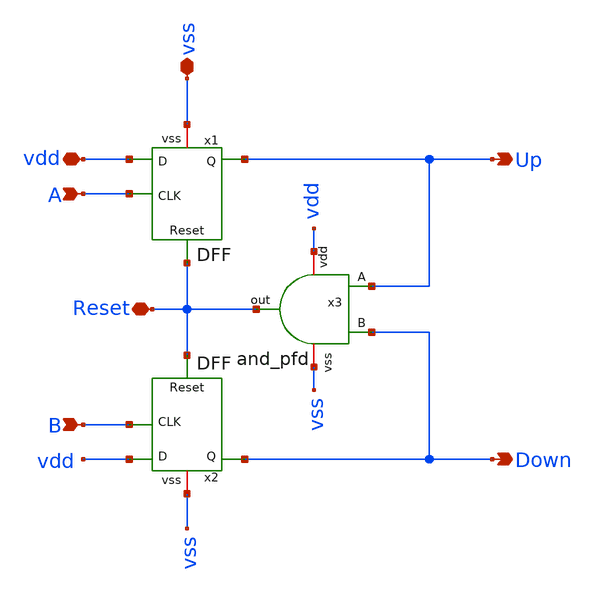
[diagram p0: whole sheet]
** sch_path: xschem/PFD.sch
**.subckt PFD vdd vss A B Down Up Reset
*.iopin vdd
*.iopin vss
*.ipin A
*.ipin B
*.opin Down
*.opin Up
*.iopin Reset
x1 vdd A Up Reset vss DFF
x2 vdd B Down Reset vss DFF
x3 vdd Reset Up Down vss and_pfd
**.ends

* expanding   symbol:  DFF.sym # of pins=5
** sym_path: xschem/DFF.sym
** sch_path: xschem/DFF.sch
.subckt DFF D CLK Q Reset vss
*.ipin D
*.ipin CLK
*.opin Q
*.ipin Reset
*.iopin vss
x1 D CLK Q P vss nor
x2 D P P1 Q vss nor
x3 D P P2 P1 vss nor
x4 D P1 Reset P2 vss nor
.ends


* expanding   symbol:  and_pfd.sym # of pins=5
** sym_path: xschem/and_pfd.sym
** sch_path: xschem/and_pfd.sch
.subckt and_pfd vdd out A B vss
*.iopin vdd
*.iopin vss
*.opin out
*.ipin A
*.ipin B
XM1 out_nand A net1 vss sky130_fd_pr__nfet_01v8 L=0.15 W=0.45 nf=1 ad='int((nf+1)/2) * W/nf * 0.29' as='int((nf+2)/2) * W/nf * 0.29'
+ pd='2*int((nf+1)/2) * (W/nf + 0.29)' ps='2*int((nf+2)/2) * (W/nf + 0.29)' nrd='0.29 / W' nrs='0.29 / W'
+ sa=0 sb=0 sd=0 mult=1 m=1
XM2 out_nand A vdd vdd sky130_fd_pr__pfet_01v8 L=0.15 W=0.9 nf=1 ad='int((nf+1)/2) * W/nf * 0.29' as='int((nf+2)/2) * W/nf * 0.29'
+ pd='2*int((nf+1)/2) * (W/nf + 0.29)' ps='2*int((nf+2)/2) * (W/nf + 0.29)' nrd='0.29 / W' nrs='0.29 / W'
+ sa=0 sb=0 sd=0 mult=1 m=1
XM3 net1 B vss vss sky130_fd_pr__nfet_01v8 L=0.15 W=0.45 nf=1 ad='int((nf+1)/2) * W/nf * 0.29' as='int((nf+2)/2) * W/nf * 0.29'
+ pd='2*int((nf+1)/2) * (W/nf + 0.29)' ps='2*int((nf+2)/2) * (W/nf + 0.29)' nrd='0.29 / W' nrs='0.29 / W'
+ sa=0 sb=0 sd=0 mult=1 m=1
XM4 out_nand B net2 vss sky130_fd_pr__nfet_01v8 L=0.15 W=0.45 nf=1 ad='int((nf+1)/2) * W/nf * 0.29' as='int((nf+2)/2) * W/nf * 0.29'
+ pd='2*int((nf+1)/2) * (W/nf + 0.29)' ps='2*int((nf+2)/2) * (W/nf + 0.29)' nrd='0.29 / W' nrs='0.29 / W'
+ sa=0 sb=0 sd=0 mult=1 m=1
XM5 net2 A vss vss sky130_fd_pr__nfet_01v8 L=0.15 W=0.45 nf=1 ad='int((nf+1)/2) * W/nf * 0.29' as='int((nf+2)/2) * W/nf * 0.29'
+ pd='2*int((nf+1)/2) * (W/nf + 0.29)' ps='2*int((nf+2)/2) * (W/nf + 0.29)' nrd='0.29 / W' nrs='0.29 / W'
+ sa=0 sb=0 sd=0 mult=1 m=1
XM6 out_nand B vdd vdd sky130_fd_pr__pfet_01v8 L=0.15 W=0.9 nf=1 ad='int((nf+1)/2) * W/nf * 0.29' as='int((nf+2)/2) * W/nf * 0.29'
+ pd='2*int((nf+1)/2) * (W/nf + 0.29)' ps='2*int((nf+2)/2) * (W/nf + 0.29)' nrd='0.29 / W' nrs='0.29 / W'
+ sa=0 sb=0 sd=0 mult=1 m=1
XM7 out out_nand vdd vdd sky130_fd_pr__pfet_01v8 L=0.15 W=0.9 nf=1 ad='int((nf+1)/2) * W/nf * 0.29' as='int((nf+2)/2) * W/nf * 0.29'
+ pd='2*int((nf+1)/2) * (W/nf + 0.29)' ps='2*int((nf+2)/2) * (W/nf + 0.29)' nrd='0.29 / W' nrs='0.29 / W'
+ sa=0 sb=0 sd=0 mult=1 m=1
XM8 out out_nand vss vss sky130_fd_pr__nfet_01v8 L=0.15 W=0.45 nf=1 ad='int((nf+1)/2) * W/nf * 0.29'
+ as='int((nf+2)/2) * W/nf * 0.29' pd='2*int((nf+1)/2) * (W/nf + 0.29)' ps='2*int((nf+2)/2) * (W/nf + 0.29)'
+ nrd='0.29 / W' nrs='0.29 / W' sa=0 sb=0 sd=0 mult=1 m=1
.ends


* expanding   symbol:  nor.sym # of pins=5
** sym_path: xschem/nor.sym
** sch_path: xschem/nor.sch
.subckt nor vdd A B out vss
*.ipin A
*.ipin B
*.iopin vdd
*.opin out
*.iopin vss
XM1 out A vss vss sky130_fd_pr__nfet_01v8 L=0.15 W=0.45 nf=1 ad='int((nf+1)/2) * W/nf * 0.29' as='int((nf+2)/2) * W/nf * 0.29'
+ pd='2*int((nf+1)/2) * (W/nf + 0.29)' ps='2*int((nf+2)/2) * (W/nf + 0.29)' nrd='0.29 / W' nrs='0.29 / W'
+ sa=0 sb=0 sd=0 mult=1 m=1
XM2 out B vss vss sky130_fd_pr__nfet_01v8 L=0.15 W=0.45 nf=1 ad='int((nf+1)/2) * W/nf * 0.29' as='int((nf+2)/2) * W/nf * 0.29'
+ pd='2*int((nf+1)/2) * (W/nf + 0.29)' ps='2*int((nf+2)/2) * (W/nf + 0.29)' nrd='0.29 / W' nrs='0.29 / W'
+ sa=0 sb=0 sd=0 mult=1 m=1
XM4 out B net1 vdd sky130_fd_pr__pfet_01v8 L=0.15 W=0.9 nf=1 ad='int((nf+1)/2) * W/nf * 0.29' as='int((nf+2)/2) * W/nf * 0.29'
+ pd='2*int((nf+1)/2) * (W/nf + 0.29)' ps='2*int((nf+2)/2) * (W/nf + 0.29)' nrd='0.29 / W' nrs='0.29 / W'
+ sa=0 sb=0 sd=0 mult=1 m=1
XM3 net1 A vdd vdd sky130_fd_pr__pfet_01v8 L=0.15 W=0.9 nf=1 ad='int((nf+1)/2) * W/nf * 0.29' as='int((nf+2)/2) * W/nf * 0.29'
+ pd='2*int((nf+1)/2) * (W/nf + 0.29)' ps='2*int((nf+2)/2) * (W/nf + 0.29)' nrd='0.29 / W' nrs='0.29 / W'
+ sa=0 sb=0 sd=0 mult=1 m=1
XM5 net2 B vdd vdd sky130_fd_pr__pfet_01v8 L=0.15 W=0.9 nf=1 ad='int((nf+1)/2) * W/nf * 0.29' as='int((nf+2)/2) * W/nf * 0.29'
+ pd='2*int((nf+1)/2) * (W/nf + 0.29)' ps='2*int((nf+2)/2) * (W/nf + 0.29)' nrd='0.29 / W' nrs='0.29 / W'
+ sa=0 sb=0 sd=0 mult=1 m=1
XM6 out A net2 vdd sky130_fd_pr__pfet_01v8 L=0.15 W=0.9 nf=1 ad='int((nf+1)/2) * W/nf * 0.29' as='int((nf+2)/2) * W/nf * 0.29'
+ pd='2*int((nf+1)/2) * (W/nf + 0.29)' ps='2*int((nf+2)/2) * (W/nf + 0.29)' nrd='0.29 / W' nrs='0.29 / W'
+ sa=0 sb=0 sd=0 mult=1 m=1
.ends

.end
